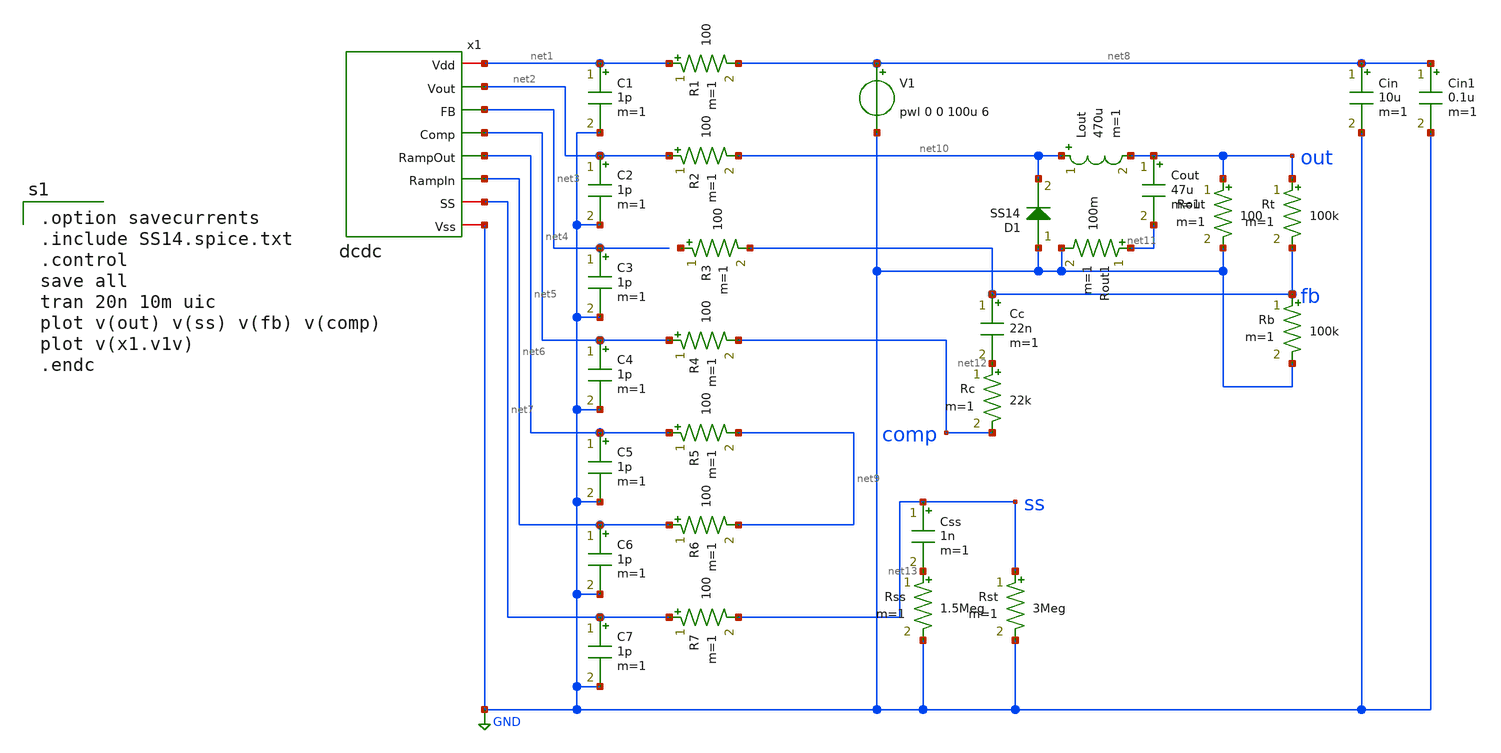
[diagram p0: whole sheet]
** sch_path: member_project/DCDC/xschem/dcdc_tran.sch
**.subckt dcdc_tran
x1 net1 net7 net2 net6 net3 net5 GND net4 dcdc
C1 net1 GND 1p m=1
R1 net1 net8 100 m=1
V1 net8 GND pwl 0 0 100u 6
D1 GND net10 SS14 area=1
Lout net10 out 470u m=1
Cout out net11 47u m=1
Rout out GND 100 m=1
Rt out fb 100k m=1
Rb fb GND 100k m=1
Rc net12 comp 22k m=1
Cc fb net12 22n m=1
Css ss net13 1n m=1
Rss net13 GND 1.5Meg m=1
Rst ss GND 3Meg m=1
Rout1 net11 GND 100m m=1
Cin net8 GND 10u m=1
Cin1 net8 GND 0.1u m=1
C2 net2 GND 1p m=1
C3 net3 GND 1p m=1
C4 net4 GND 1p m=1
C5 net5 GND 1p m=1
C6 net6 GND 1p m=1
C7 net7 GND 1p m=1
R2 net2 net10 100 m=1
R3 net14 fb 100 m=1
R4 net4 comp 100 m=1
R5 net5 net9 100 m=1
R6 net6 net9 100 m=1
R7 net7 ss 100 m=1
**** begin user architecture code
 .include $::LIB/ip62_models

.option savecurrents
.include SS14.spice.txt
.control
save all
tran 20n 10m uic
plot v(out) v(ss) v(fb) v(comp)
plot v(x1.v1v)
.endc

**** end user architecture code
**.ends
.GLOBAL GND
.end
